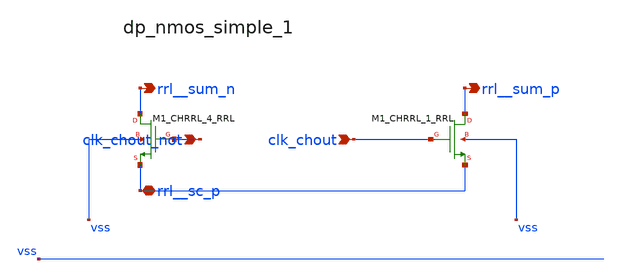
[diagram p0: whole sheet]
** sch_path: analog-db/raw/ia_004_fan_chopper_rrl/hier/blocks/dp_nmos_simple_1.sch
**.subckt dp_nmos_simple_1 clk_chout_not clk_chout rrl__sc_p rrl__sum_n rrl__sum_p
*.ipin clk_chout_not
*.ipin clk_chout
*.iopin rrl__sc_p
*.opin rrl__sum_n
*.opin rrl__sum_p
XM1_CHRRL_1_RRL rrl__sum_p clk_chout rrl__sc_p vss sg13_lv_nmos w=x_dut_xm1_chrrl_1_rrl_w
+ l=x_dut_xm1_chrrl_1_rrl_l ng=1 m=x_dut_xm1_chrrl_1_rrl_m
XM1_CHRRL_4_RRL rrl__sum_n clk_chout_not rrl__sc_p vss sg13_lv_nmos w=x_dut_xm1_chrrl_4_rrl_w
+ l=x_dut_xm1_chrrl_4_rrl_l ng=1 m=x_dut_xm1_chrrl_4_rrl_m
**.ends
.end
